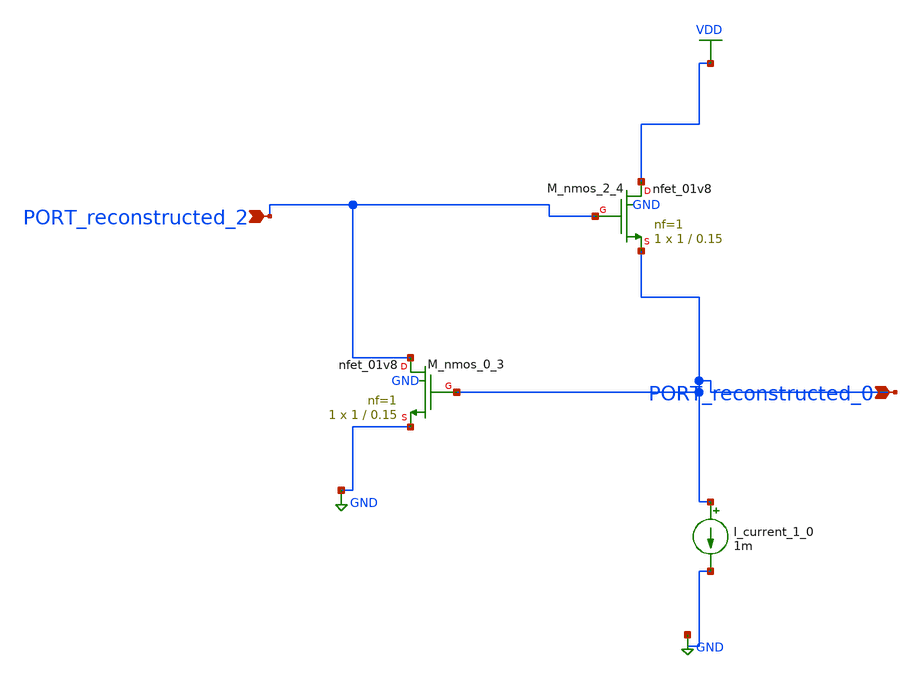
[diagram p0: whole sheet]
** sch_path: schematics/AMSNet/524.sch
**.subckt 524 PORT_reconstructed_0 PORT_reconstructed_2
*.ipin PORT_reconstructed_0
*.ipin PORT_reconstructed_2
I_current_1_0 PORT_reconstructed_0 GND 1m
XM_nmos_0_3 PORT_reconstructed_2 PORT_reconstructed_0 GND GND sky130_fd_pr__nfet_01v8 L=0.15 W=1 nf=1
+ ad='int((1 + 1)/2) * 1 / 1 * 0.29' as='int((1 + 2)/2) * 1 / 1 * 0.29' pd='2*int((1 + 1)/2) * (1 / 1 + 0.29)'
+ ps='2*int((1 + 2)/2) * (1 / 1 + 0.29)' nrd='0.29 / 1 ' nrs='0.29 / 1 ' sa=0 sb=0 sd=0 mult=1 m=1
XM_nmos_2_4 VDD PORT_reconstructed_2 PORT_reconstructed_0 GND sky130_fd_pr__nfet_01v8 L=0.15 W=1 nf=1
+ ad='int((1 + 1)/2) * 1 / 1 * 0.29' as='int((1 + 2)/2) * 1 / 1 * 0.29' pd='2*int((1 + 1)/2) * (1 / 1 + 0.29)'
+ ps='2*int((1 + 2)/2) * (1 / 1 + 0.29)' nrd='0.29 / 1 ' nrs='0.29 / 1 ' sa=0 sb=0 sd=0 mult=1 m=1
**.ends
.GLOBAL GND
.GLOBAL VDD
.end
